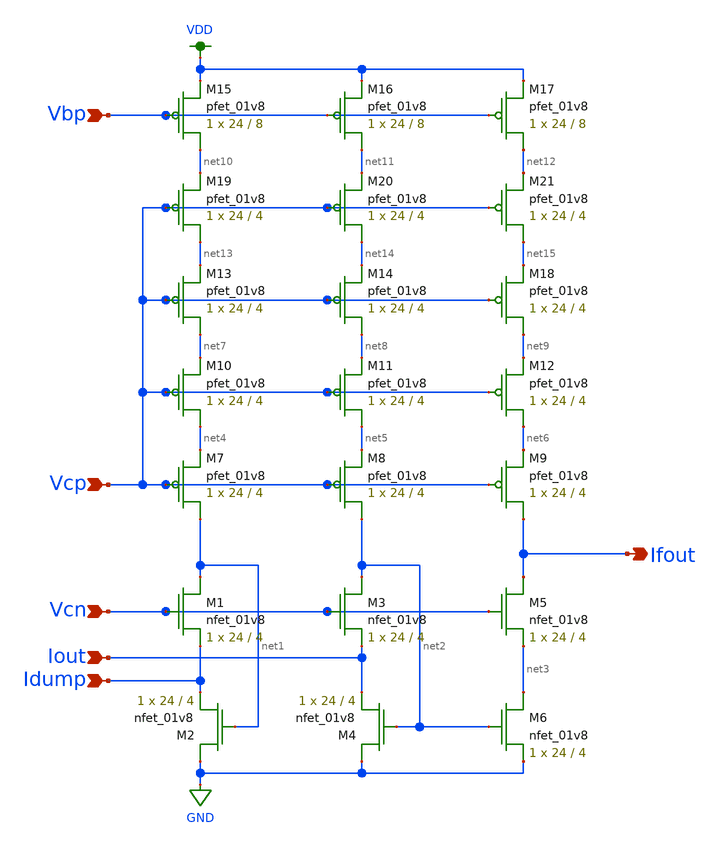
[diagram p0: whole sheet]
** sch_path: xschem/FVF-1.sch
**.subckt FVF-1 Vcn Iout Idump Vcp Vbp Ifout
*.ipin Vcn
*.ipin Iout
*.ipin Idump
*.ipin Vcp
*.ipin Vbp
*.opin Ifout
XM1 net1 Vcn Idump GND sky130_fd_pr__nfet_01v8 L=4 W=24 nf=1 ad='int((nf+1)/2) * W/nf * 0.29' as='int((nf+2)/2) * W/nf * 0.29'
+ pd='2*int((nf+1)/2) * (W/nf + 0.29)' ps='2*int((nf+2)/2) * (W/nf + 0.29)' nrd='0.29 / W' nrs='0.29 / W'
+ sa=0 sb=0 sd=0 mult=1 m=1
XM2 GND net1 Idump GND sky130_fd_pr__nfet_01v8 L=4 W=24 nf=1 ad='int((nf+1)/2) * W/nf * 0.29' as='int((nf+2)/2) * W/nf * 0.29'
+ pd='2*int((nf+1)/2) * (W/nf + 0.29)' ps='2*int((nf+2)/2) * (W/nf + 0.29)' nrd='0.29 / W' nrs='0.29 / W'
+ sa=0 sb=0 sd=0 mult=1 m=1
XM3 net2 Vcn Iout GND sky130_fd_pr__nfet_01v8 L=4 W=24 nf=1 ad='int((nf+1)/2) * W/nf * 0.29' as='int((nf+2)/2) * W/nf * 0.29'
+ pd='2*int((nf+1)/2) * (W/nf + 0.29)' ps='2*int((nf+2)/2) * (W/nf + 0.29)' nrd='0.29 / W' nrs='0.29 / W'
+ sa=0 sb=0 sd=0 mult=1 m=1
XM4 GND net2 Iout GND sky130_fd_pr__nfet_01v8 L=4 W=24 nf=1 ad='int((nf+1)/2) * W/nf * 0.29' as='int((nf+2)/2) * W/nf * 0.29'
+ pd='2*int((nf+1)/2) * (W/nf + 0.29)' ps='2*int((nf+2)/2) * (W/nf + 0.29)' nrd='0.29 / W' nrs='0.29 / W'
+ sa=0 sb=0 sd=0 mult=1 m=1
XM5 Ifout Vcn net3 GND sky130_fd_pr__nfet_01v8 L=4 W=24 nf=1 ad='int((nf+1)/2) * W/nf * 0.29' as='int((nf+2)/2) * W/nf * 0.29'
+ pd='2*int((nf+1)/2) * (W/nf + 0.29)' ps='2*int((nf+2)/2) * (W/nf + 0.29)' nrd='0.29 / W' nrs='0.29 / W'
+ sa=0 sb=0 sd=0 mult=1 m=1
XM6 net3 net2 GND GND sky130_fd_pr__nfet_01v8 L=4 W=24 nf=1 ad='int((nf+1)/2) * W/nf * 0.29' as='int((nf+2)/2) * W/nf * 0.29'
+ pd='2*int((nf+1)/2) * (W/nf + 0.29)' ps='2*int((nf+2)/2) * (W/nf + 0.29)' nrd='0.29 / W' nrs='0.29 / W'
+ sa=0 sb=0 sd=0 mult=1 m=1
XM7 net1 Vcp net4 VDD sky130_fd_pr__pfet_01v8 L=4 W=24 nf=1 ad='int((nf+1)/2) * W/nf * 0.29' as='int((nf+2)/2) * W/nf * 0.29'
+ pd='2*int((nf+1)/2) * (W/nf + 0.29)' ps='2*int((nf+2)/2) * (W/nf + 0.29)' nrd='0.29 / W' nrs='0.29 / W'
+ sa=0 sb=0 sd=0 mult=1 m=1
XM8 net2 Vcp net5 VDD sky130_fd_pr__pfet_01v8 L=4 W=24 nf=1 ad='int((nf+1)/2) * W/nf * 0.29' as='int((nf+2)/2) * W/nf * 0.29'
+ pd='2*int((nf+1)/2) * (W/nf + 0.29)' ps='2*int((nf+2)/2) * (W/nf + 0.29)' nrd='0.29 / W' nrs='0.29 / W'
+ sa=0 sb=0 sd=0 mult=1 m=1
XM9 Ifout Vcp net6 VDD sky130_fd_pr__pfet_01v8 L=4 W=24 nf=1 ad='int((nf+1)/2) * W/nf * 0.29' as='int((nf+2)/2) * W/nf * 0.29'
+ pd='2*int((nf+1)/2) * (W/nf + 0.29)' ps='2*int((nf+2)/2) * (W/nf + 0.29)' nrd='0.29 / W' nrs='0.29 / W'
+ sa=0 sb=0 sd=0 mult=1 m=1
XM15 net10 Vbp VDD VDD sky130_fd_pr__pfet_01v8 L=8 W=24 nf=1 ad='int((nf+1)/2) * W/nf * 0.29' as='int((nf+2)/2) * W/nf * 0.29'
+ pd='2*int((nf+1)/2) * (W/nf + 0.29)' ps='2*int((nf+2)/2) * (W/nf + 0.29)' nrd='0.29 / W' nrs='0.29 / W'
+ sa=0 sb=0 sd=0 mult=1 m=1
XM16 net11 Vbp VDD VDD sky130_fd_pr__pfet_01v8 L=8 W=24 nf=1 ad='int((nf+1)/2) * W/nf * 0.29' as='int((nf+2)/2) * W/nf * 0.29'
+ pd='2*int((nf+1)/2) * (W/nf + 0.29)' ps='2*int((nf+2)/2) * (W/nf + 0.29)' nrd='0.29 / W' nrs='0.29 / W'
+ sa=0 sb=0 sd=0 mult=1 m=1
XM17 net12 Vbp VDD VDD sky130_fd_pr__pfet_01v8 L=8 W=24 nf=1 ad='int((nf+1)/2) * W/nf * 0.29' as='int((nf+2)/2) * W/nf * 0.29'
+ pd='2*int((nf+1)/2) * (W/nf + 0.29)' ps='2*int((nf+2)/2) * (W/nf + 0.29)' nrd='0.29 / W' nrs='0.29 / W'
+ sa=0 sb=0 sd=0 mult=1 m=1
XM10 net4 Vcp net7 VDD sky130_fd_pr__pfet_01v8 L=4 W=24 nf=1 ad='int((nf+1)/2) * W/nf * 0.29' as='int((nf+2)/2) * W/nf * 0.29'
+ pd='2*int((nf+1)/2) * (W/nf + 0.29)' ps='2*int((nf+2)/2) * (W/nf + 0.29)' nrd='0.29 / W' nrs='0.29 / W'
+ sa=0 sb=0 sd=0 mult=1 m=1
XM11 net5 Vcp net8 VDD sky130_fd_pr__pfet_01v8 L=4 W=24 nf=1 ad='int((nf+1)/2) * W/nf * 0.29' as='int((nf+2)/2) * W/nf * 0.29'
+ pd='2*int((nf+1)/2) * (W/nf + 0.29)' ps='2*int((nf+2)/2) * (W/nf + 0.29)' nrd='0.29 / W' nrs='0.29 / W'
+ sa=0 sb=0 sd=0 mult=1 m=1
XM12 net6 Vcp net9 VDD sky130_fd_pr__pfet_01v8 L=4 W=24 nf=1 ad='int((nf+1)/2) * W/nf * 0.29' as='int((nf+2)/2) * W/nf * 0.29'
+ pd='2*int((nf+1)/2) * (W/nf + 0.29)' ps='2*int((nf+2)/2) * (W/nf + 0.29)' nrd='0.29 / W' nrs='0.29 / W'
+ sa=0 sb=0 sd=0 mult=1 m=1
XM13 net7 Vcp net13 VDD sky130_fd_pr__pfet_01v8 L=4 W=24 nf=1 ad='int((nf+1)/2) * W/nf * 0.29' as='int((nf+2)/2) * W/nf * 0.29'
+ pd='2*int((nf+1)/2) * (W/nf + 0.29)' ps='2*int((nf+2)/2) * (W/nf + 0.29)' nrd='0.29 / W' nrs='0.29 / W'
+ sa=0 sb=0 sd=0 mult=1 m=1
XM14 net8 Vcp net14 VDD sky130_fd_pr__pfet_01v8 L=4 W=24 nf=1 ad='int((nf+1)/2) * W/nf * 0.29' as='int((nf+2)/2) * W/nf * 0.29'
+ pd='2*int((nf+1)/2) * (W/nf + 0.29)' ps='2*int((nf+2)/2) * (W/nf + 0.29)' nrd='0.29 / W' nrs='0.29 / W'
+ sa=0 sb=0 sd=0 mult=1 m=1
XM18 net9 Vcp net15 VDD sky130_fd_pr__pfet_01v8 L=4 W=24 nf=1 ad='int((nf+1)/2) * W/nf * 0.29' as='int((nf+2)/2) * W/nf * 0.29'
+ pd='2*int((nf+1)/2) * (W/nf + 0.29)' ps='2*int((nf+2)/2) * (W/nf + 0.29)' nrd='0.29 / W' nrs='0.29 / W'
+ sa=0 sb=0 sd=0 mult=1 m=1
XM19 net13 Vcp net10 VDD sky130_fd_pr__pfet_01v8 L=4 W=24 nf=1 ad='int((nf+1)/2) * W/nf * 0.29' as='int((nf+2)/2) * W/nf * 0.29'
+ pd='2*int((nf+1)/2) * (W/nf + 0.29)' ps='2*int((nf+2)/2) * (W/nf + 0.29)' nrd='0.29 / W' nrs='0.29 / W'
+ sa=0 sb=0 sd=0 mult=1 m=1
XM20 net14 Vcp net11 VDD sky130_fd_pr__pfet_01v8 L=4 W=24 nf=1 ad='int((nf+1)/2) * W/nf * 0.29' as='int((nf+2)/2) * W/nf * 0.29'
+ pd='2*int((nf+1)/2) * (W/nf + 0.29)' ps='2*int((nf+2)/2) * (W/nf + 0.29)' nrd='0.29 / W' nrs='0.29 / W'
+ sa=0 sb=0 sd=0 mult=1 m=1
XM21 net15 Vcp net12 VDD sky130_fd_pr__pfet_01v8 L=4 W=24 nf=1 ad='int((nf+1)/2) * W/nf * 0.29' as='int((nf+2)/2) * W/nf * 0.29'
+ pd='2*int((nf+1)/2) * (W/nf + 0.29)' ps='2*int((nf+2)/2) * (W/nf + 0.29)' nrd='0.29 / W' nrs='0.29 / W'
+ sa=0 sb=0 sd=0 mult=1 m=1
**.ends
.GLOBAL VDD
.GLOBAL GND
.end
